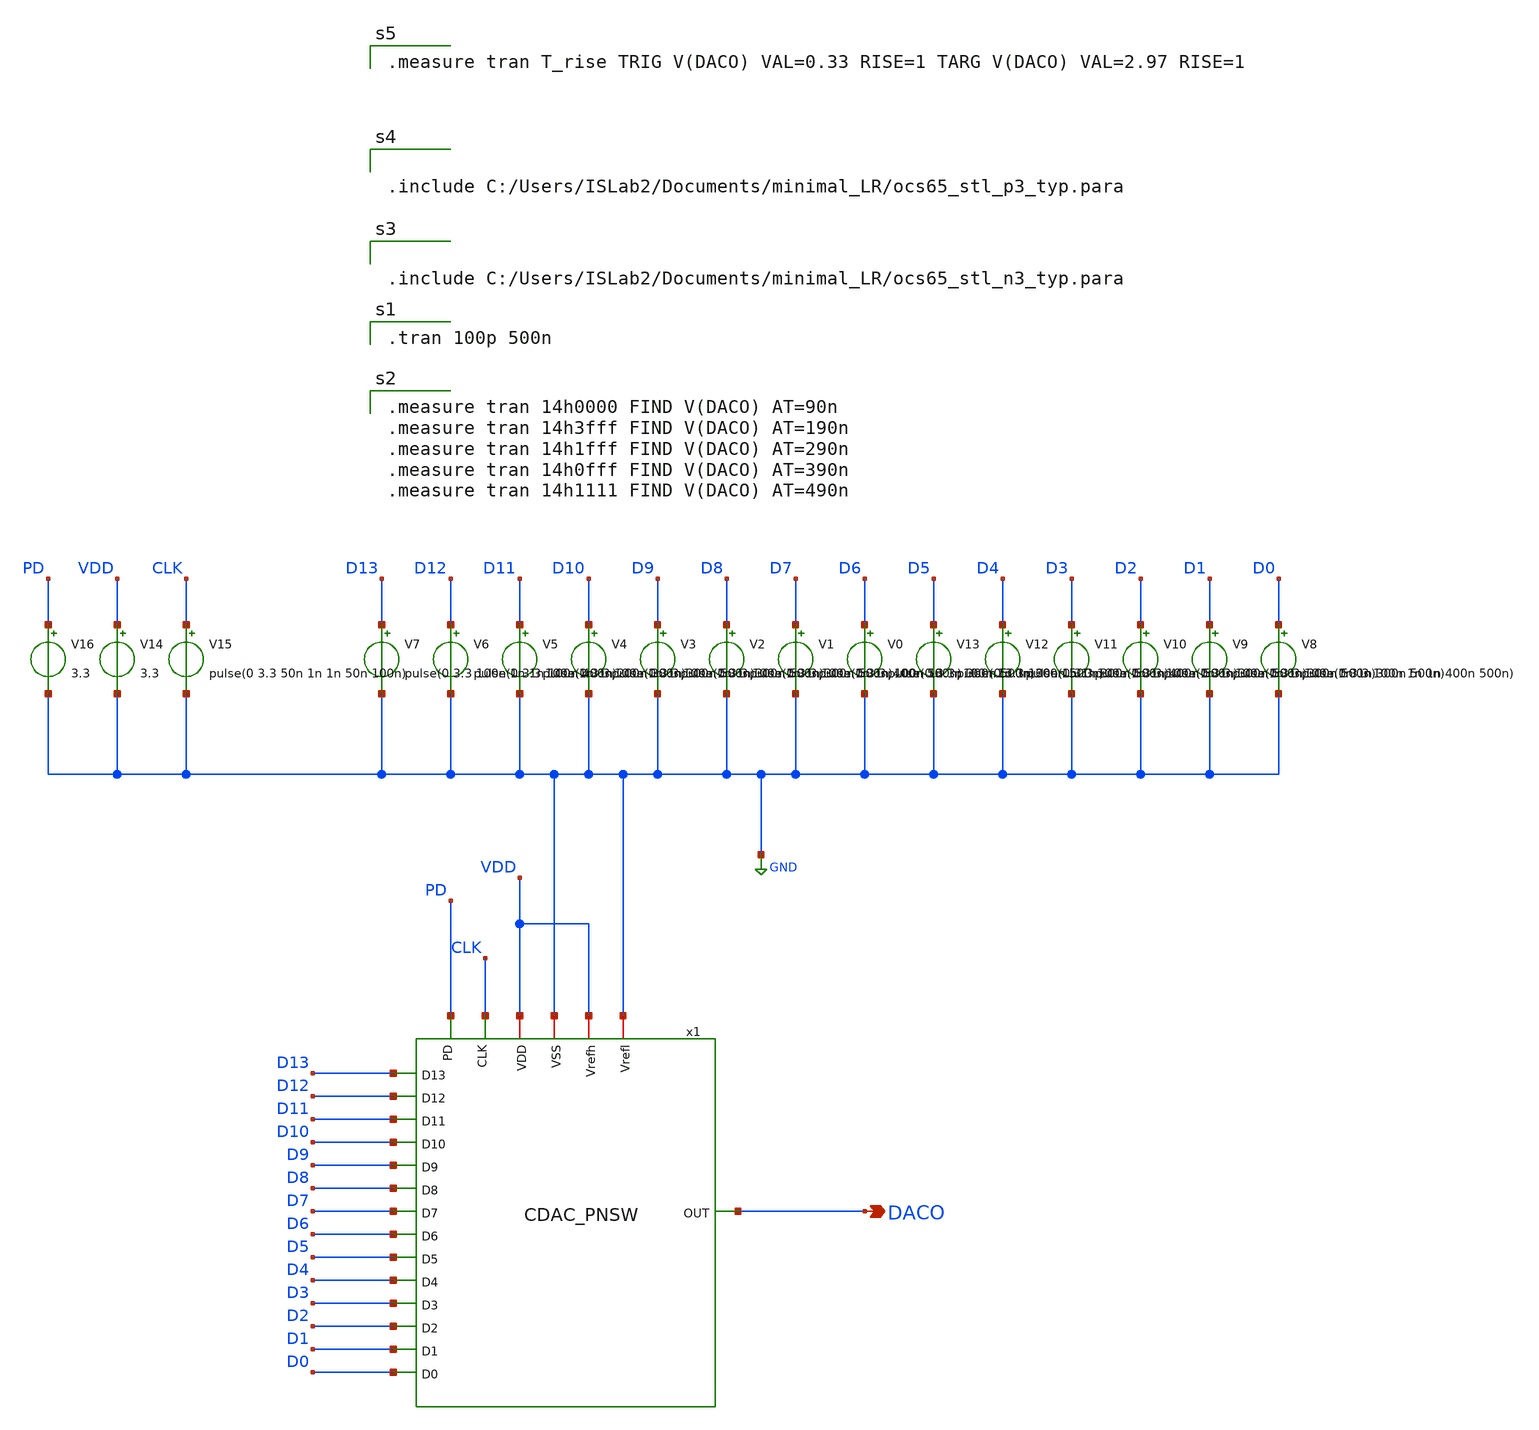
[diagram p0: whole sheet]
** sch_path: CDAC_sim.sch
**.subckt CDAC_sim DACO
*.opin DACO
V14 VDD GND 3.3
V15 CLK GND pulse(0 3.3 50n 1n 1n 50n 100n)
x1 CLK D11 D13 D12 D7 D10 D1 D0 D9 D8 D2 D6 D5 D4 D3 DACO GND VDD GND VDD PD CDAC_PNSW
V16 PD GND 3.3
V13 D5 GND pulse(0 3.3 100n 1n 1n 300n 500n)
V12 D4 GND pulse(0 3.3 100n 1n 1n 400n 500n)
V11 D3 GND pulse(0 3.3 100n 1n 1n 300n 500n)
V10 D2 GND pulse(0 3.3 100n 1n 1n 300n 500n)
V9 D1 GND pulse(0 3.3 100n 1n 1n 300n 500n)
V8 D0 GND pulse(0 3.3 100n 1n 1n 400n 500n)
V7 D13 GND pulse(0 3.3 100n 1n 1n 100n 400n)
V6 D12 GND pulse(0 3.3 100n 1n 1n 200n 300n)
V5 D11 GND pulse(0 3.3 100n 1n 1n 300n 500n)
V4 D10 GND pulse(0 3.3 100n 1n 1n 300n 500n)
V3 D9 GND pulse(0 3.3 100n 1n 1n 300n 500n)
V2 D8 GND pulse(0 3.3 100n 1n 1n 400n 500n)
V1 D7 GND pulse(0 3.3 100n 1n 1n 300n 500n)
V0 D6 GND pulse(0 3.3 100n 1n 1n 300n 500n)
**** begin user architecture code

.tran 100p 500n


.measure tran 14h0000 FIND V(DACO) AT=90n
.measure tran 14h3fff FIND V(DACO) AT=190n
.measure tran 14h1fff FIND V(DACO) AT=290n
.measure tran 14h0fff FIND V(DACO) AT=390n
.measure tran 14h1111 FIND V(DACO) AT=490n



.include C:/Users/ISLab2/Documents/minimal_LR/ocs65_stl_n3_typ.para



.include C:/Users/ISLab2/Documents/minimal_LR/ocs65_stl_p3_typ.para


.measure tran T_rise TRIG V(DACO) VAL=0.33 RISE=1 TARG V(DACO) VAL=2.97 RISE=1

**** end user architecture code
**.ends

* expanding   symbol:  CDAC_PNSW.sym # of pins=21
** sym_path: CDAC_PNSW.sym
** sch_path: CDAC_PNSW.sch
.subckt CDAC_PNSW CLK D11 D13 D12 D7 D10 D1 D0 D9 D8 D2 D6 D5 D4 D3 OUT VSS VDD Vrefl Vrefh PD
*.opin OUT
*.iopin Vrefh
*.iopin Vrefl
*.ipin D13
*.ipin D12
*.ipin D11
*.ipin D10
*.iopin VSS
*.iopin VDD
*.ipin D9
*.ipin D8
*.ipin D7
*.ipin D6
*.ipin D5
*.ipin D4
*.ipin D3
*.ipin D2
*.ipin D1
*.ipin D0
*.ipin CLK
*.ipin PD
C1 OUT Vrefl 33f m=1
C2 OUT net1 33f m=1
C3 OUT net2 66f m=1
C4 OUT net4 132f m=1
C5 OUT net3 264f m=1
x15 VDD D13b D13 VSS INV
x16 VDD D12b D12 VSS INV
x17 VDD D11b D11 VSS INV
x18 VDD D10b D10 VSS INV
C6 OUT net5 528f m=1
C7 OUT net6 1.056p m=1
C8 OUT net8 2.112p m=1
C9 OUT net7 4.224p m=1
C10 OUT net10 8.448p m=1
C11 OUT net9 16.896p m=1
C12 OUT net11 33.792p m=1
C13 OUT net12 67.584p m=1
C14 OUT net14 135.168p m=1
C15 OUT net13 270.336p m=1
x34 VDD D9b D9 VSS INV
x35 VDD D8b D8 VSS INV
x36 VDD D7b D7 VSS INV
x37 VDD D6b D6 VSS INV
x38 VDD D5b D5 VSS INV
x39 VDD D4b D4 VSS INV
x40 VDD D3b D3 VSS INV
x41 VDD D2b D2 VSS INV
x42 VDD D1b D1 VSS INV
x43 VDD D0b D0 VSS INV
x44 VDD D13A CLK2 D13 VSS AND
x45 VDD D12A CLK2 D12 VSS AND
x46 VDD D11A CLK2 D11 VSS AND
x47 VDD D10A CLK2 D10 VSS AND
x48 VDD D9A CLK2 D9 VSS AND
x49 VDD D8A CLK2 D8 VSS AND
x50 VDD D7A CLK2 D7 VSS AND
x51 VDD D6A CLK2 D6 VSS AND
x52 VDD D5A CLK2 D5 VSS AND
x53 VDD D4A CLK2 D4 VSS AND
x54 VDD D3A CLK2 D3 VSS AND
x55 VDD D2A CLK2 D2 VSS AND
x56 VDD D1A CLK2 D1 VSS AND
x57 VDD D0A CLK2 D0 VSS AND
x58 VDD CLK1 D13bO D13b VSS OR
x59 VDD CLK1 D12bO D12b VSS OR
x60 VDD CLK1 D11bO D11b VSS OR
x61 VDD CLK1 D10bO D10b VSS OR
x62 VDD CLK1 D9bO D9b VSS OR
x63 VDD CLK1 D8bO D8b VSS OR
x64 VDD CLK1 D7bO D7b VSS OR
x65 VDD CLK1 D6bO D6b VSS OR
x66 VDD CLK1 D5bO D5b VSS OR
x67 VDD CLK1 D4bO D4b VSS OR
x68 VDD CLK1 D3bO D3b VSS OR
x69 VDD CLK1 D2bO D2b VSS OR
x70 VDD CLK1 D1bO D1b VSS OR
x71 VDD CLK1 D0bO D0b VSS OR
x72 VDD CLK CLK1 VSS net15 NOL
x31 D13bO VSS net13 Vrefl NMOSSW16
x33 D12bO VSS net14 Vrefl NMOSSW8
x29 D11bO VSS net12 Vrefl NMOSSW4
x27 D10bO VSS net11 Vrefl NMOSSW2
x1 resetPD VSS OUT Vrefl NMOSSW16
x2 D0bO VSS net1 Vrefl NMOSSW
x4 D1bO VSS net2 Vrefl NMOSSW
x6 D2bO VSS net4 Vrefl NMOSSW
x8 D3bO VSS net3 Vrefl NMOSSW
x10 D4bO VSS net5 Vrefl NMOSSW
x12 D5bO VSS net6 Vrefl NMOSSW
x14 D6bO VSS net8 Vrefl NMOSSW
x20 D7bO VSS net7 Vrefl NMOSSW
x22 D8bO VSS net10 Vrefl NMOSSW
x24 D9bO VSS net9 Vrefl NMOSSW
x3 D13A net13 Vrefh VDD PMOSSW16
x5 D12A net14 Vrefh VDD PMOSSW8
x7 D11A net12 Vrefh VDD PMOSSW4
x9 D10A net11 Vrefh VDD PMOSSW2
x11 D9A net9 Vrefh VDD PMOSSW
x13 D8A net10 Vrefh VDD PMOSSW
x19 D7A net7 Vrefh VDD PMOSSW
x21 D6A net8 Vrefh VDD PMOSSW
x23 D5A net6 Vrefh VDD PMOSSW
x25 D4A net5 Vrefh VDD PMOSSW
x26 D3A net3 Vrefh VDD PMOSSW
x28 D2A net4 Vrefh VDD PMOSSW
x30 D1A net2 Vrefh VDD PMOSSW
x32 D0A net1 Vrefh VDD PMOSSW
x73 VDD CLK2 net15 VSS INV
x74 VDD net16 PD VSS INV
x75 VDD CLK1 resetPD net16 VSS OR
.ends


* expanding   symbol:  INV.sym # of pins=4
** sym_path: INV.sym
** sch_path: INV.sch
.subckt INV VDD OUT IN VSS
*.opin OUT
*.ipin IN
*.iopin VDD
*.iopin VSS
M2 OUT IN VDD VDD pch w=10u l=0.35u as=0 ps=0 ad=0 pd=0 m=1
M1 OUT IN VSS VSS nch w=5u l=0.35u as=0 ps=0 ad=0 pd=0 m=1
.ends


* expanding   symbol:  AND.sym # of pins=5
** sym_path: AND.sym
** sch_path: AND.sch
.subckt AND VDD Y A B VSS
*.iopin VDD
*.ipin A
*.ipin B
*.iopin VSS
*.opin Y
M1 net1 A net2 VSS nch w=3.5u l=0.35u as=0 ps=0 ad=0 pd=0 m=1
M2 net1 B VDD VDD pch w=3.5u l=0.35u as=0 ps=0 ad=0 pd=0 m=1
M3 net1 A VDD VDD pch w=3.5u l=0.35u as=0 ps=0 ad=0 pd=0 m=1
M4 net2 B VSS VSS nch w=3.5u l=0.35u as=0 ps=0 ad=0 pd=0 m=1
M5 Y net1 VDD VDD pch w=3.5u l=0.35u as=0 ps=0 ad=0 pd=0 m=1
M6 Y net1 VSS VSS nch w=3.5u l=0.35u as=0 ps=0 ad=0 pd=0 m=1
.ends


* expanding   symbol:  OR.sym # of pins=5
** sym_path: OR.sym
** sch_path: OR.sch
.subckt OR VDD A Y B VSS
*.iopin VDD
*.ipin A
*.ipin B
*.iopin VSS
*.opin Y
M1 net1 A VSS VSS nch w=3.5u l=0.35u as=0 ps=0 ad=0 pd=0 m=1
M2 net2 A VDD VDD pch w=3.5u l=0.35u as=0 ps=0 ad=0 pd=0 m=1
M3 net1 B net2 VDD pch w=3.5u l=0.35u as=0 ps=0 ad=0 pd=0 m=1
M4 net1 B VSS VSS nch w=3.5u l=0.35u as=0 ps=0 ad=0 pd=0 m=1
M5 Y net1 VDD VDD pch w=3.5u l=0.35u as=0 ps=0 ad=0 pd=0 m=1
M6 Y net1 VSS VSS nch w=3.5u l=0.35u as=0 ps=0 ad=0 pd=0 m=1
.ends


* expanding   symbol:  NOL.sym # of pins=5
** sym_path: NOL.sym
** sch_path: NOL.sch
.subckt NOL VDD CLK CLK1 VSS CLK2
*.ipin CLK
*.opin CLK1
*.opin CLK2
*.iopin VDD
*.iopin VSS
x3 VDD net1 CLK VSS INV
x1 VDD CLK net9 CLK2 VSS NOR
x2 VDD CLK1 net2 net1 VSS NOR
x4 VDD net3 net2 VSS INV
x5 VDD net4 net3 VSS INV
x6 VDD net5 net4 VSS INV
x7 VDD net17 net5 VSS INV
x8 VDD net6 net9 VSS INV
x9 VDD net7 net6 VSS INV
x10 VDD net8 net7 VSS INV
x11 VDD net13 net8 VSS INV
x12 VDD net10 net13 VSS INV
x13 VDD net11 net10 VSS INV
x14 VDD net12 net11 VSS INV
x15 VDD net32 net12 VSS INV
x16 VDD net14 net17 VSS INV
x17 VDD net15 net14 VSS INV
x18 VDD net16 net15 VSS INV
x19 VDD net33 net16 VSS INV
x20 VDD net18 net33 VSS INV
x21 VDD net19 net18 VSS INV
x22 VDD net20 net19 VSS INV
x23 VDD net24 net20 VSS INV
x24 VDD net21 net24 VSS INV
x25 VDD net22 net21 VSS INV
x26 VDD net23 net22 VSS INV
x27 VDD net34 net23 VSS INV
x28 VDD net25 net32 VSS INV
x29 VDD net26 net25 VSS INV
x30 VDD net27 net26 VSS INV
x31 VDD net31 net27 VSS INV
x32 VDD net28 net31 VSS INV
x33 VDD net29 net28 VSS INV
x34 VDD net30 net29 VSS INV
x35 VDD net50 net30 VSS INV
x36 VDD net35 net34 VSS INV
x37 VDD net36 net35 VSS INV
x38 VDD net37 net36 VSS INV
x39 VDD net41 net37 VSS INV
x40 VDD net38 net41 VSS INV
x41 VDD net39 net38 VSS INV
x42 VDD net40 net39 VSS INV
x43 VDD net42 net40 VSS INV
x44 VDD net43 net50 VSS INV
x45 VDD net44 net43 VSS INV
x46 VDD net45 net44 VSS INV
x47 VDD net49 net45 VSS INV
x48 VDD net46 net49 VSS INV
x49 VDD net47 net46 VSS INV
x50 VDD net48 net47 VSS INV
x51 VDD net61 net48 VSS INV
x52 VDD net51 net42 VSS INV
x53 VDD net53 net51 VSS INV
x54 VDD net52 net61 VSS INV
x55 VDD net60 net52 VSS INV
x56 VDD net54 net53 VSS INV
x57 VDD net55 net54 VSS INV
x58 VDD net56 net55 VSS INV
x59 VDD CLK2 net56 VSS INV
x64 VDD net57 net60 VSS INV
x65 VDD net58 net57 VSS INV
x66 VDD net59 net58 VSS INV
x67 VDD CLK1 net59 VSS INV
.ends


* expanding   symbol:  NMOSSW16.sym # of pins=4
** sym_path: NMOSSW16.sym
** sch_path: NMOSSW16.sch
.subckt NMOSSW16 CLK VSS OUT IN
*.ipin IN
*.opin OUT
*.iopin VSS
*.iopin CLK
x1 CLK VSS OUT IN NMOSSW8
x2 CLK VSS OUT IN NMOSSW8
.ends


* expanding   symbol:  NMOSSW8.sym # of pins=4
** sym_path: NMOSSW8.sym
** sch_path: NMOSSW8.sch
.subckt NMOSSW8 CLK VSS OUT IN
*.ipin IN
*.opin OUT
*.iopin VSS
*.iopin CLK
x1 CLK VSS OUT IN NMOSSW4
x2 CLK VSS OUT IN NMOSSW4
.ends


* expanding   symbol:  NMOSSW4.sym # of pins=4
** sym_path: NMOSSW4.sym
** sch_path: NMOSSW4.sch
.subckt NMOSSW4 CLK VSS OUT IN
*.ipin IN
*.opin OUT
*.iopin VSS
*.iopin CLK
x1 CLK VSS OUT IN NMOSSW2
x2 CLK VSS OUT IN NMOSSW2
.ends


* expanding   symbol:  NMOSSW2.sym # of pins=4
** sym_path: NMOSSW2.sym
** sch_path: NMOSSW2.sch
.subckt NMOSSW2 CLK VSS OUT IN
*.ipin IN
*.opin OUT
*.iopin VSS
*.iopin CLK
x1 CLK VSS OUT IN NMOSSW
x2 CLK VSS OUT IN NMOSSW
.ends


* expanding   symbol:  NMOSSW.sym # of pins=4
** sym_path: NMOSSW.sym
** sch_path: NMOSSW.sch
.subckt NMOSSW CLK VSS OUT IN
*.ipin IN
*.iopin VSS
*.opin OUT
*.iopin CLK
M1 OUT CLK IN VSS nch w=20u l=0.35u as=0 ps=0 ad=0 pd=0 m=1
.ends


* expanding   symbol:  PMOSSW16.sym # of pins=4
** sym_path: PMOSSW16.sym
** sch_path: PMOSSW16.sch
.subckt PMOSSW16 CLK OUT IN VDD
*.ipin IN
*.opin OUT
*.iopin CLK
*.iopin VDD
x1 CLK OUT IN VDD PMOSSW8
x2 CLK OUT IN VDD PMOSSW8
.ends


* expanding   symbol:  PMOSSW8.sym # of pins=4
** sym_path: PMOSSW8.sym
** sch_path: PMOSSW8.sch
.subckt PMOSSW8 CLK OUT IN VDD
*.ipin IN
*.opin OUT
*.iopin CLK
*.iopin VDD
x1 CLK OUT IN VDD PMOSSW4
x2 CLK OUT IN VDD PMOSSW4
.ends


* expanding   symbol:  PMOSSW4.sym # of pins=4
** sym_path: PMOSSW4.sym
** sch_path: PMOSSW4.sch
.subckt PMOSSW4 CLK OUT IN VDD
*.ipin IN
*.opin OUT
*.iopin CLK
*.iopin VDD
x1 CLK OUT IN VDD PMOSSW2
x2 CLK OUT IN VDD PMOSSW2
.ends


* expanding   symbol:  PMOSSW2.sym # of pins=4
** sym_path: PMOSSW2.sym
** sch_path: PMOSSW2.sch
.subckt PMOSSW2 CLK OUT IN VDD
*.ipin IN
*.opin OUT
*.iopin CLK
*.iopin VDD
x1 CLK OUT IN VDD PMOSSW
x2 CLK OUT IN VDD PMOSSW
.ends


* expanding   symbol:  PMOSSW.sym # of pins=4
** sym_path: PMOSSW.sym
** sch_path: PMOSSW.sch
.subckt PMOSSW CLK OUT IN VDD
*.ipin IN
*.opin OUT
*.iopin VDD
*.iopin CLK
M5 OUT CLK IN VDD pch w=20u l=0.35u as=0 ps=0 ad=0 pd=0 m=1
.ends


* expanding   symbol:  NOR.sym # of pins=5
** sym_path: NOR.sym
** sch_path: NOR.sch
.subckt NOR VDD A Y B VSS
*.iopin VDD
*.ipin A
*.ipin B
*.iopin VSS
*.opin Y
M1 Y A VSS VSS nch w=3.5u l=0.35u as=0 ps=0 ad=0 pd=0 m=1
M2 net1 A VDD VDD pch w=3.5u l=0.35u as=0 ps=0 ad=0 pd=0 m=1
M3 Y B net1 VDD pch w=3.5u l=0.35u as=0 ps=0 ad=0 pd=0 m=1
M4 Y B VSS VSS nch w=3.5u l=0.35u as=0 ps=0 ad=0 pd=0 m=1
.ends

.GLOBAL GND
.end
